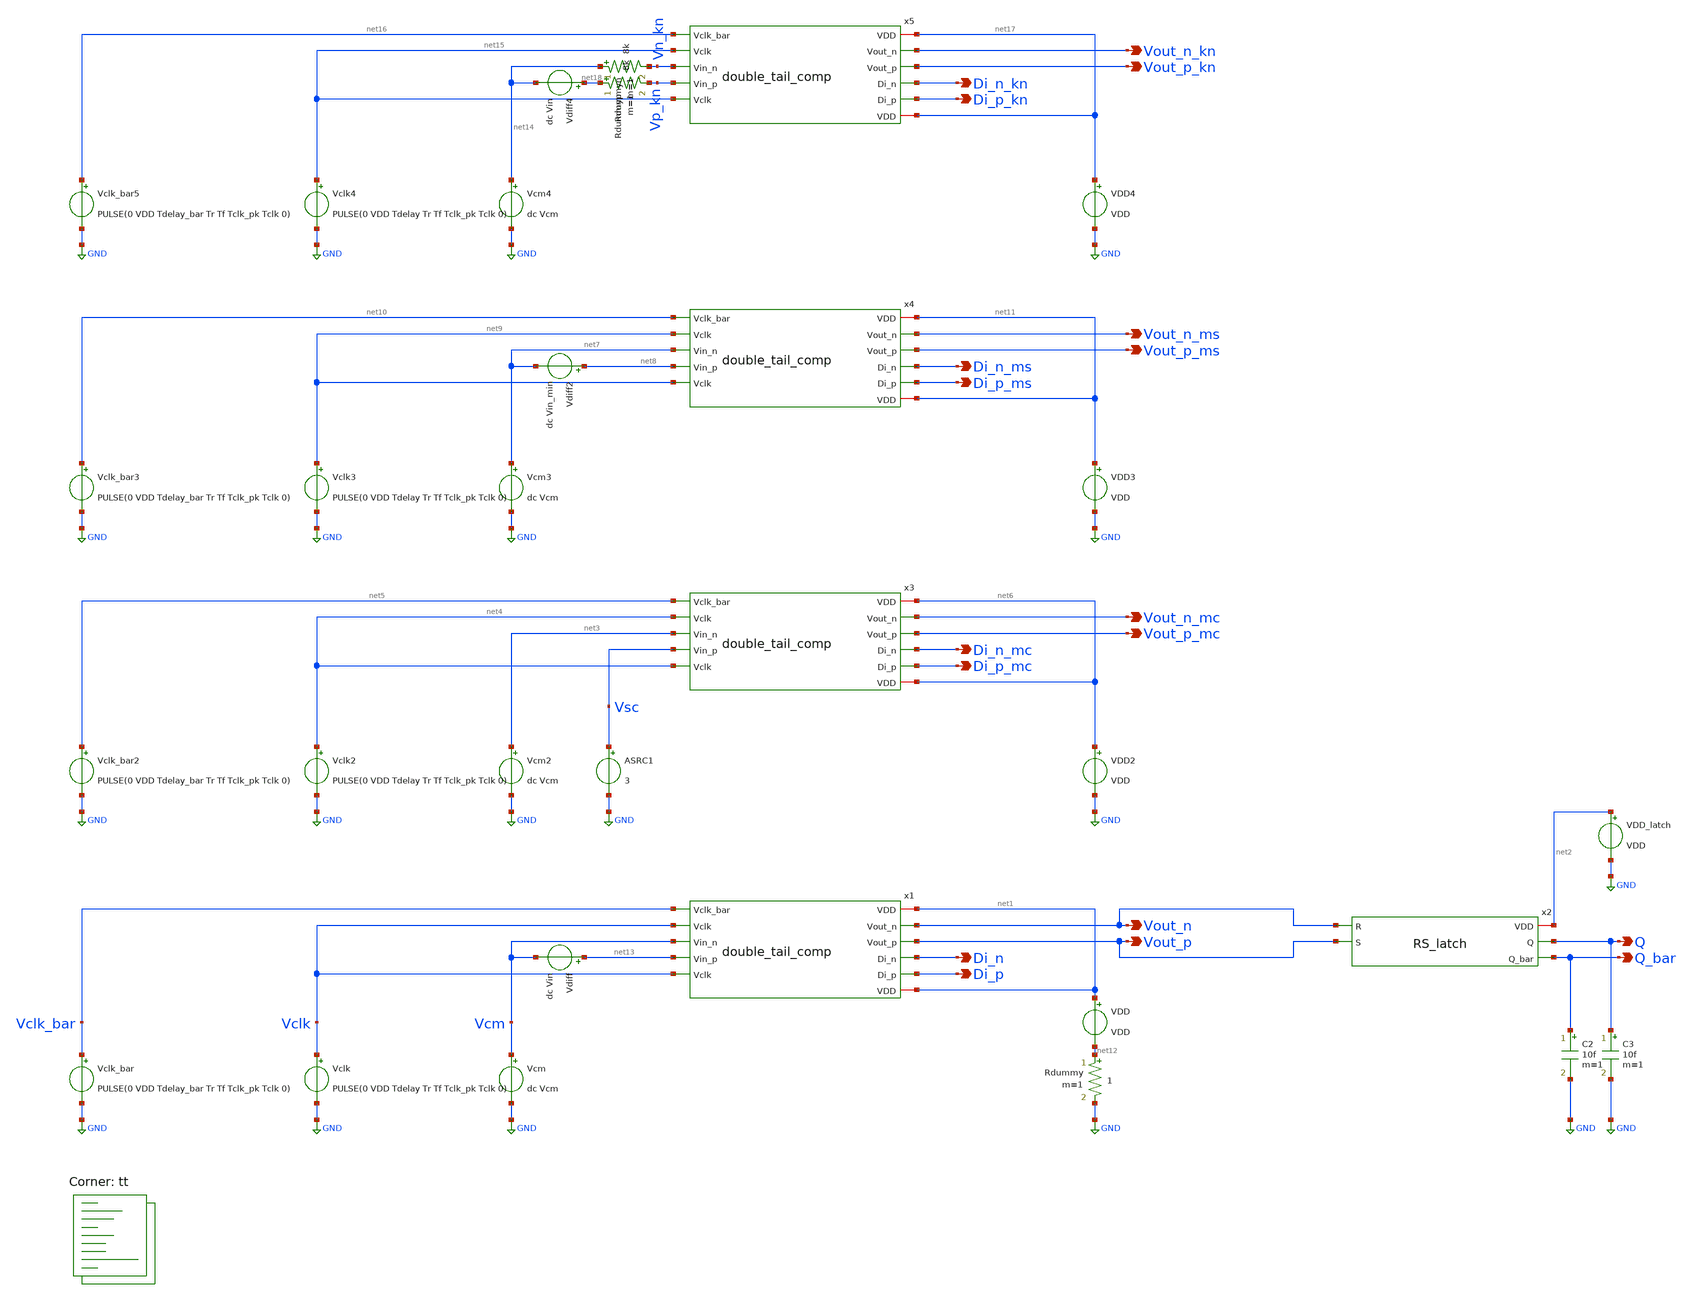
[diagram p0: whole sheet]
** sch_path: xschem/double_tail_comp_tb.sch
**.subckt double_tail_comp_tb Di_n Di_p Vout_n Vout_p Q Q_bar Di_n_mc Di_p_mc Vout_n_mc Vout_p_mc
*+ Di_n_ms Di_p_ms Vout_n_ms Vout_p_ms Di_n_kn Di_p_kn Vout_n_kn Vout_p_kn
*.opin Di_n
*.opin Di_p
*.opin Vout_n
*.opin Vout_p
*.opin Q
*.opin Q_bar
*.opin Di_n_mc
*.opin Di_p_mc
*.opin Vout_n_mc
*.opin Vout_p_mc
*.opin Di_n_ms
*.opin Di_p_ms
*.opin Vout_n_ms
*.opin Vout_p_ms
*.opin Di_n_kn
*.opin Di_p_kn
*.opin Vout_n_kn
*.opin Vout_p_kn
x1 net1 Vclk_bar Vout_n Vout_p Di_n Di_p Vclk Vcm net13 double_tail_comp
VDD net1 net12 VDD
Vclk Vclk GND PULSE(0 VDD Tdelay Tr Tf Tclk_pk Tclk 0)
Vclk_bar Vclk_bar GND PULSE(0 VDD Tdelay_bar Tr Tf Tclk_pk Tclk 0)
Vcm Vcm GND dc Vcm
Vdiff net13 Vcm dc Vin
C2 Q_bar GND 10f m=1
C3 Q GND 10f m=1
x2 net2 Vout_n Q Vout_p Q_bar RS_latch
x3 net6 net5 Vout_n_mc Vout_p_mc Di_n_mc Di_p_mc net4 net3 Vsc double_tail_comp
VDD2 net6 GND VDD
Vclk2 net4 GND PULSE(0 VDD Tdelay Tr Tf Tclk_pk Tclk 0)
Vclk_bar2 net5 GND PULSE(0 VDD Tdelay_bar Tr Tf Tclk_pk Tclk 0)
Vcm2 net3 GND dc Vcm
ASRC1 %v([ Vsc ]) filesrc
x4 net11 net10 Vout_n_ms Vout_p_ms Di_n_ms Di_p_ms net9 net7 net8 double_tail_comp
VDD3 net11 GND VDD
Vclk3 net9 GND PULSE(0 VDD Tdelay Tr Tf Tclk_pk Tclk 0)
Vclk_bar3 net10 GND PULSE(0 VDD Tdelay_bar Tr Tf Tclk_pk Tclk 0)
Vcm3 net7 GND dc Vcm
Vdiff2 net8 net7 dc Vin_min
VDD_latch net2 GND VDD
Rdummy net12 GND 1 m=1
x5 net17 net16 Vout_n_kn Vout_p_kn Di_n_kn Di_p_kn net15 Vn_kn Vp_kn double_tail_comp
VDD4 net17 GND VDD
Vclk4 net15 GND PULSE(0 VDD Tdelay Tr Tf Tclk_pk Tclk 0)
Vclk_bar5 net16 GND PULSE(0 VDD Tdelay_bar Tr Tf Tclk_pk Tclk 0)
Vcm4 net14 GND dc Vcm
Vdiff4 net18 net14 dc Vin
Rdummyn net14 Vn_kn 8k m=1
Rdummyp net18 Vp_kn 8k m=1
**** begin user architecture code
.lib $::SKYWATER_MODELS/sky130.lib.spice tt


*.OPTIONS maxord=1
*.OPTIONS itl1=200
*.OPTIONS itl2=200
*.OPTIONS itl4=200

* save all voltage and current
.save all
.options savecurrents
.options seed=random

.nodeset V(Vout_n) = 0
.nodeset V(Vout_p) = 0
.nodeset V(Di_n) = 0
.nodeset V(Di_p) = 0
.nodeset V(Q) = 0
.nodeset V(Q_bar) = 0

.nodeset V(Vout_n_mc) = 0
.nodeset V(Vout_p_mc) = 0
.nodeset V(Di_n_mc) = 0
.nodeset V(Di_p_mc) = 0

.nodeset V(Vout_n_ms) = 0
.nodeset V(Vout_p_ms) = 0
.nodeset V(Di_n_ms) = 0
.nodeset V(Di_p_ms) = 0

.control
set filetype=ascii
set units=degrees

.include /autofs/fs1.ece/fs1.eecg.tcc/lizongh2/sky130_comparator/xschem/simulations/double_tail_comp_tb_vars.spice
.include /autofs/fs1.ece/fs1.eecg.tcc/lizongh2/sky130_comparator/xschem/simulations/double_tail_comp_tb_analyses.spice

.endc


**** end user architecture code
**.ends

* expanding   symbol:  double_tail_comp.sym # of pins=11
** sym_path: xschem/double_tail_comp.sym
** sch_path: xschem/double_tail_comp.sch
.subckt double_tail_comp VDD Vclk_bar Vout_n Vout_p Di_n Di_p Vclk Vin_n Vin_p
*.iopin VDD
*.ipin Vclk
*.ipin Vclk
*.ipin Vin_p
*.ipin Vin_n
*.opin Di_n
*.opin Di_p
*.opin Vout_n
*.opin Vout_p
*.ipin Vclk_bar
*.iopin VDD
XM1 Di_n Vin_p net1 GND sky130_fd_pr__nfet_01v8 L=0.18 W=W_M1 nf=1 ad='int((nf+1)/2) * W/nf * 0.29' as='int((nf+2)/2) * W/nf * 0.29'
+ pd='2*int((nf+1)/2) * (W/nf + 0.29)' ps='2*int((nf+2)/2) * (W/nf + 0.29)' nrd='0.29 / W' nrs='0.29 / W'
+ sa=0 sb=0 sd=0 mult=1 m=1
XM2 Di_p Vin_n net1 GND sky130_fd_pr__nfet_01v8 L=0.18 W=W_M2 nf=1 ad='int((nf+1)/2) * W/nf * 0.29' as='int((nf+2)/2) * W/nf * 0.29'
+ pd='2*int((nf+1)/2) * (W/nf + 0.29)' ps='2*int((nf+2)/2) * (W/nf + 0.29)' nrd='0.29 / W' nrs='0.29 / W'
+ sa=0 sb=0 sd=0 mult=1 m=1
XM3 Di_n Vclk VDD VDD sky130_fd_pr__pfet_01v8 L=0.18 W=W_M3 nf=1 ad='int((nf+1)/2) * W/nf * 0.29' as='int((nf+2)/2) * W/nf * 0.29'
+ pd='2*int((nf+1)/2) * (W/nf + 0.29)' ps='2*int((nf+2)/2) * (W/nf + 0.29)' nrd='0.29 / W' nrs='0.29 / W'
+ sa=0 sb=0 sd=0 mult=1 m=1
XM4 Di_p Vclk VDD VDD sky130_fd_pr__pfet_01v8 L=0.18 W=W_M4 nf=1 ad='int((nf+1)/2) * W/nf * 0.29' as='int((nf+2)/2) * W/nf * 0.29'
+ pd='2*int((nf+1)/2) * (W/nf + 0.29)' ps='2*int((nf+2)/2) * (W/nf + 0.29)' nrd='0.29 / W' nrs='0.29 / W'
+ sa=0 sb=0 sd=0 mult=1 m=1
XM5 net1 Vclk GND GND sky130_fd_pr__nfet_01v8 L=0.18 W=W_M5 nf=1 ad='int((nf+1)/2) * W/nf * 0.29' as='int((nf+2)/2) * W/nf * 0.29'
+ pd='2*int((nf+1)/2) * (W/nf + 0.29)' ps='2*int((nf+2)/2) * (W/nf + 0.29)' nrd='0.29 / W' nrs='0.29 / W'
+ sa=0 sb=0 sd=0 mult=1 m=1
XM6 Vout_p Di_n GND GND sky130_fd_pr__nfet_01v8 L=0.18 W=W_M6 nf=1 ad='int((nf+1)/2) * W/nf * 0.29' as='int((nf+2)/2) * W/nf * 0.29'
+ pd='2*int((nf+1)/2) * (W/nf + 0.29)' ps='2*int((nf+2)/2) * (W/nf + 0.29)' nrd='0.29 / W' nrs='0.29 / W'
+ sa=0 sb=0 sd=0 mult=1 m=1
XM7 Vout_p Vout_n GND GND sky130_fd_pr__nfet_01v8 L=0.18 W=W_M7 nf=1 ad='int((nf+1)/2) * W/nf * 0.29'
+ as='int((nf+2)/2) * W/nf * 0.29' pd='2*int((nf+1)/2) * (W/nf + 0.29)' ps='2*int((nf+2)/2) * (W/nf + 0.29)'
+ nrd='0.29 / W' nrs='0.29 / W' sa=0 sb=0 sd=0 mult=1 m=1
XM8 Vout_n Vout_p GND GND sky130_fd_pr__nfet_01v8 L=0.18 W=W_M8 nf=1 ad='int((nf+1)/2) * W/nf * 0.29'
+ as='int((nf+2)/2) * W/nf * 0.29' pd='2*int((nf+1)/2) * (W/nf + 0.29)' ps='2*int((nf+2)/2) * (W/nf + 0.29)'
+ nrd='0.29 / W' nrs='0.29 / W' sa=0 sb=0 sd=0 mult=1 m=1
XM9 Vout_n Di_p GND GND sky130_fd_pr__nfet_01v8 L=0.18 W=W_M9 nf=1 ad='int((nf+1)/2) * W/nf * 0.29' as='int((nf+2)/2) * W/nf * 0.29'
+ pd='2*int((nf+1)/2) * (W/nf + 0.29)' ps='2*int((nf+2)/2) * (W/nf + 0.29)' nrd='0.29 / W' nrs='0.29 / W'
+ sa=0 sb=0 sd=0 mult=1 m=1
XM10 Vout_p Vout_n net2 VDD sky130_fd_pr__pfet_01v8 L=0.18 W=W_M10 nf=1 ad='int((nf+1)/2) * W/nf * 0.29'
+ as='int((nf+2)/2) * W/nf * 0.29' pd='2*int((nf+1)/2) * (W/nf + 0.29)' ps='2*int((nf+2)/2) * (W/nf + 0.29)'
+ nrd='0.29 / W' nrs='0.29 / W' sa=0 sb=0 sd=0 mult=1 m=1
XM11 Vout_n Vout_p net2 VDD sky130_fd_pr__pfet_01v8 L=0.18 W=W_M11 nf=1 ad='int((nf+1)/2) * W/nf * 0.29'
+ as='int((nf+2)/2) * W/nf * 0.29' pd='2*int((nf+1)/2) * (W/nf + 0.29)' ps='2*int((nf+2)/2) * (W/nf + 0.29)'
+ nrd='0.29 / W' nrs='0.29 / W' sa=0 sb=0 sd=0 mult=1 m=1
XM12 net2 Vclk_bar VDD VDD sky130_fd_pr__pfet_01v8 L=0.18 W=W_M12 nf=1 ad='int((nf+1)/2) * W/nf * 0.29'
+ as='int((nf+2)/2) * W/nf * 0.29' pd='2*int((nf+1)/2) * (W/nf + 0.29)' ps='2*int((nf+2)/2) * (W/nf + 0.29)'
+ nrd='0.29 / W' nrs='0.29 / W' sa=0 sb=0 sd=0 mult=1 m=1
.ends


* expanding   symbol:  RS_latch.sym # of pins=5
** sym_path: xschem/RS_latch.sym
** sch_path: xschem/RS_latch.sch
.subckt RS_latch VDD R Q S Q_bar
*.iopin VDD
*.opin Q
*.opin Q_bar
*.ipin R
*.ipin S
x1 VDD R Q_bar Q nor
x2 VDD Q S Q_bar nor
.ends


* expanding   symbol:  nor.sym # of pins=4
** sym_path: xschem/nor.sym
** sch_path: xschem/nor.sch
.subckt nor VDD A B out
*.iopin VDD
*.ipin A
*.ipin B
*.opin out
XM1 out B GND GND sky130_fd_pr__nfet_01v8 L=0.18 W=0.42 nf=1 ad='int((nf+1)/2) * W/nf * 0.29' as='int((nf+2)/2) * W/nf * 0.29'
+ pd='2*int((nf+1)/2) * (W/nf + 0.29)' ps='2*int((nf+2)/2) * (W/nf + 0.29)' nrd='0.29 / W' nrs='0.29 / W'
+ sa=0 sb=0 sd=0 mult=1 m=1
XM2 out A GND GND sky130_fd_pr__nfet_01v8 L=0.18 W=0.42 nf=1 ad='int((nf+1)/2) * W/nf * 0.29' as='int((nf+2)/2) * W/nf * 0.29'
+ pd='2*int((nf+1)/2) * (W/nf + 0.29)' ps='2*int((nf+2)/2) * (W/nf + 0.29)' nrd='0.29 / W' nrs='0.29 / W'
+ sa=0 sb=0 sd=0 mult=1 m=1
XM3 out B net1 VDD sky130_fd_pr__pfet_01v8 L=0.18 W=0.84 nf=1 ad='int((nf+1)/2) * W/nf * 0.29' as='int((nf+2)/2) * W/nf * 0.29'
+ pd='2*int((nf+1)/2) * (W/nf + 0.29)' ps='2*int((nf+2)/2) * (W/nf + 0.29)' nrd='0.29 / W' nrs='0.29 / W'
+ sa=0 sb=0 sd=0 mult=1 m=1
XM4 net1 A VDD VDD sky130_fd_pr__pfet_01v8 L=0.18 W=0.84 nf=1 ad='int((nf+1)/2) * W/nf * 0.29' as='int((nf+2)/2) * W/nf * 0.29'
+ pd='2*int((nf+1)/2) * (W/nf + 0.29)' ps='2*int((nf+2)/2) * (W/nf + 0.29)' nrd='0.29 / W' nrs='0.29 / W'
+ sa=0 sb=0 sd=0 mult=1 m=1
.ends

.GLOBAL GND
**** begin user architecture code

.model filesrc filesource (file="staircase_voltage.txt" amploffset=[Vcm] amplscale=[1] timeoffset=0
+ timescale=1 timerelative=false amplstep=false)

**** end user architecture code
.end
